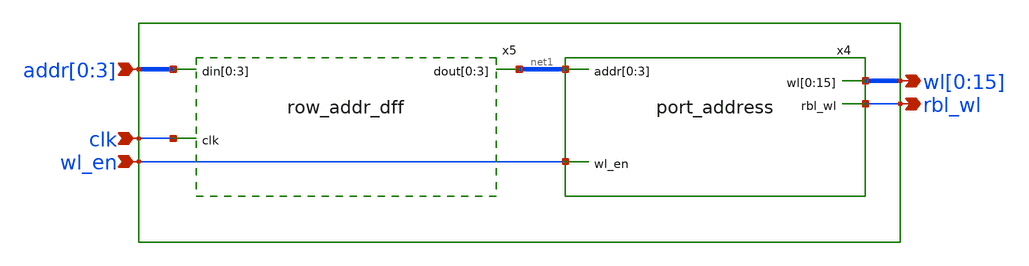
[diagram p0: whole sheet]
** sch_path: sram_2_64_scn4m_lcc/row_decoder.sch
**.subckt row_decoder addr[0],addr[1],addr[2],addr[3] clk wl_en
*+ wl[0],wl[1],wl[2],wl[3],wl[4],wl[5],wl[6],wl[7],wl[8],wl[9],wl[10],wl[11],wl[12],wl[13],wl[14],wl[15] rbl_wl
*.ipin addr[0],addr[1],addr[2],addr[3]
*.ipin clk
*.ipin wl_en
*.opin
*+ wl[0],wl[1],wl[2],wl[3],wl[4],wl[5],wl[6],wl[7],wl[8],wl[9],wl[10],wl[11],wl[12],wl[13],wl[14],wl[15]
*.opin rbl_wl
x4 net1[3] net1[2] net1[1] net1[0] wl_en wl[0] wl[1] wl[2] wl[3] wl[4] wl[5] wl[6] wl[7] wl[8] wl[9]
+ wl[10] wl[11] wl[12] wl[13] wl[14] wl[15] rbl_wl vdd gnd port_address
x5 addr[0] addr[1] addr[2] addr[3] net1[3] net1[2] net1[1] net1[0] clk vdd gnd row_addr_dff
**.ends
.end
